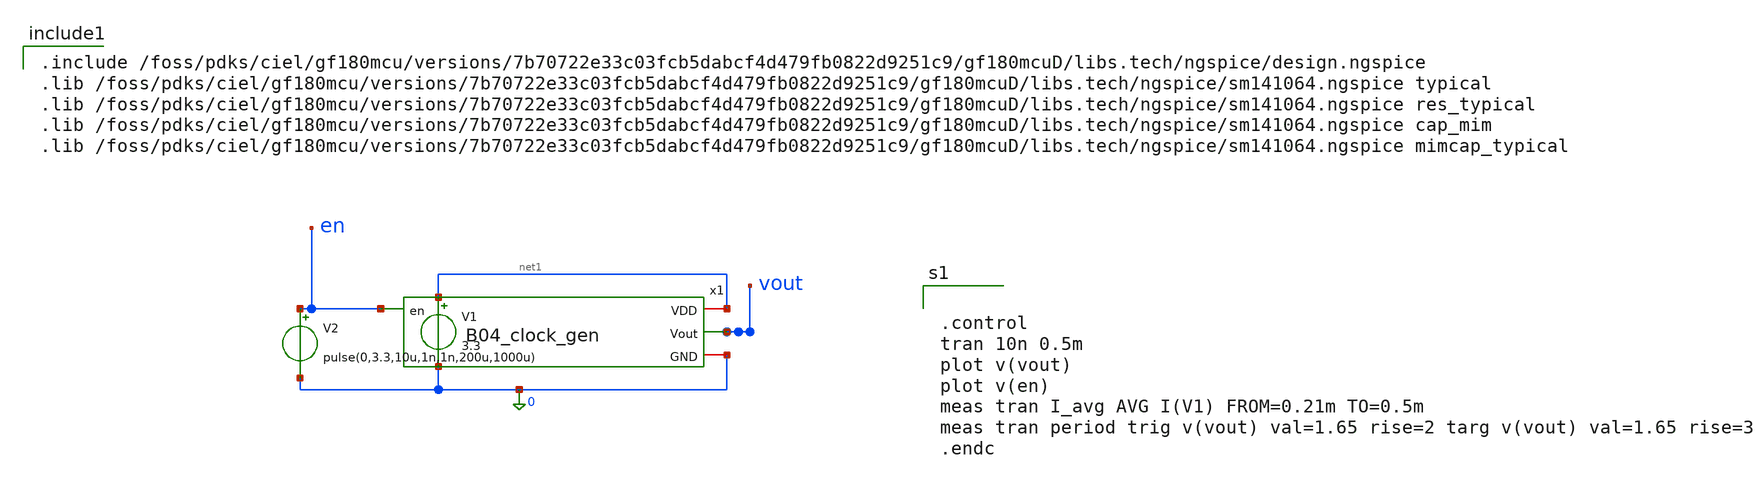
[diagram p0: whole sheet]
** sch_path: analog/clock/sch/B04_tb_clock_gen.sch
**.subckt B04_tb_clock_gen
V1 net1 0 3.3
x1 net1 vout en 0 B04_clock_gen
V2 en 0 pulse(0,3.3,10u,1n,1n,200u,1000u)
**** begin user architecture code

.include /foss/pdks/ciel/gf180mcu/versions/7b70722e33c03fcb5dabcf4d479fb0822d9251c9/gf180mcuD/libs.tech/ngspice/design.ngspice
.lib /foss/pdks/ciel/gf180mcu/versions/7b70722e33c03fcb5dabcf4d479fb0822d9251c9/gf180mcuD/libs.tech/ngspice/sm141064.ngspice typical
.lib /foss/pdks/ciel/gf180mcu/versions/7b70722e33c03fcb5dabcf4d479fb0822d9251c9/gf180mcuD/libs.tech/ngspice/sm141064.ngspice res_typical
.lib /foss/pdks/ciel/gf180mcu/versions/7b70722e33c03fcb5dabcf4d479fb0822d9251c9/gf180mcuD/libs.tech/ngspice/sm141064.ngspice cap_mim
.lib /foss/pdks/ciel/gf180mcu/versions/7b70722e33c03fcb5dabcf4d479fb0822d9251c9/gf180mcuD/libs.tech/ngspice/sm141064.ngspice mimcap_typical




.control
tran 10n 0.5m
plot v(vout)
plot v(en)
meas tran I_avg AVG I(V1) FROM=0.21m TO=0.5m
meas tran period trig v(vout) val=1.65 rise=2 targ v(vout) val=1.65 rise=3
.endc

**** end user architecture code
**.ends
.end
